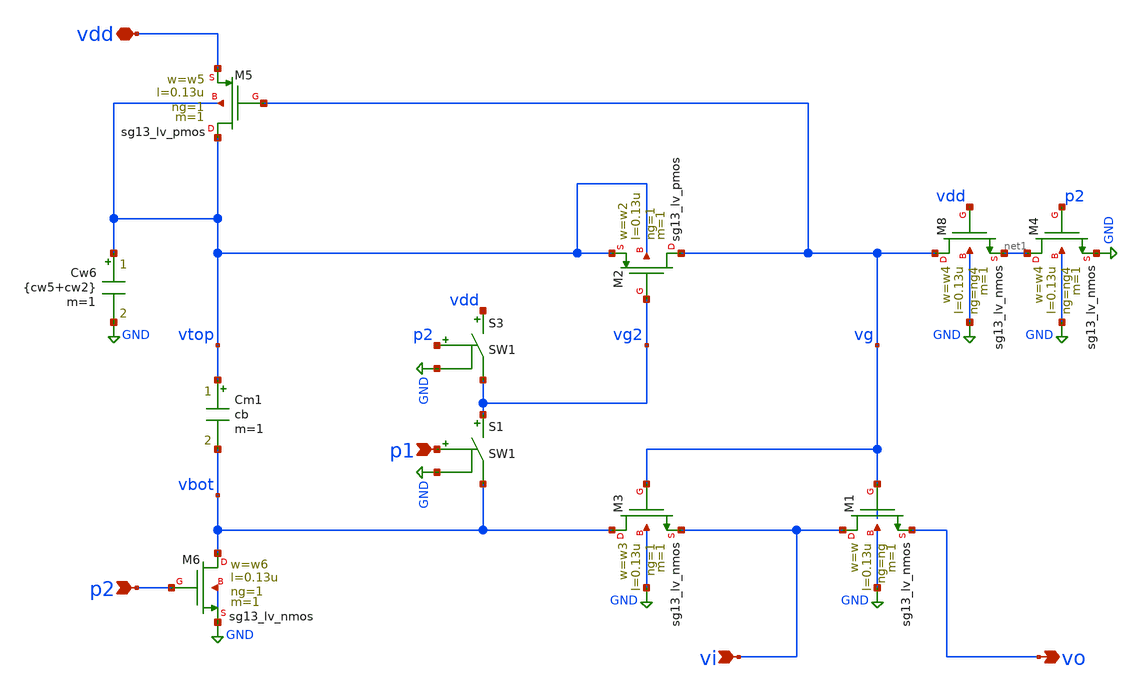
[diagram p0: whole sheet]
** sch_path: xschem/boot4.sch
**.subckt boot4 vi vo p2 vdd p1
*.ipin vi
*.opin vo
*.ipin p2
*.iopin vdd
*.ipin p1
Cm1 vtop vbot cb m=1
XM1 vi vg vo GND sg13_lv_nmos w=w l=0.13u ng=ng m=1 mm_ok=1
XM8 vg vdd net1 GND sg13_lv_nmos w=w4 l=0.13u ng=ng4 m=1 mm_ok=1
XM4 net1 p2 GND GND sg13_lv_nmos w=w4 l=0.13u ng=ng4 m=1 mm_ok=1
XM6 vbot p2 GND GND sg13_lv_nmos w=w6 l=0.13u ng=1 m=1 mm_ok=1
XM5 vtop vg vdd vtop sg13_lv_pmos w=w5 l=0.13u ng=1 m=1 mm_ok=1
Cw6 vtop GND {cw5+cw2} m=1
XM3 vbot vg vi GND sg13_lv_nmos w=w3 l=0.13u ng=1 m=1 mm_ok=1
S3 vdd vg2 p2 GND SW1
XM2 vg vg2 vtop vtop sg13_lv_pmos w=w2 l=0.13u ng=1 m=1 mm_ok=1
S1 vg2 vbot p1 GND SW1
**.ends
.GLOBAL GND
**** begin user architecture code
.MODEL SW1 SW   VT=0.6 VH=vh  RON=rsw ROFF=roff
**** end user architecture code
.end
